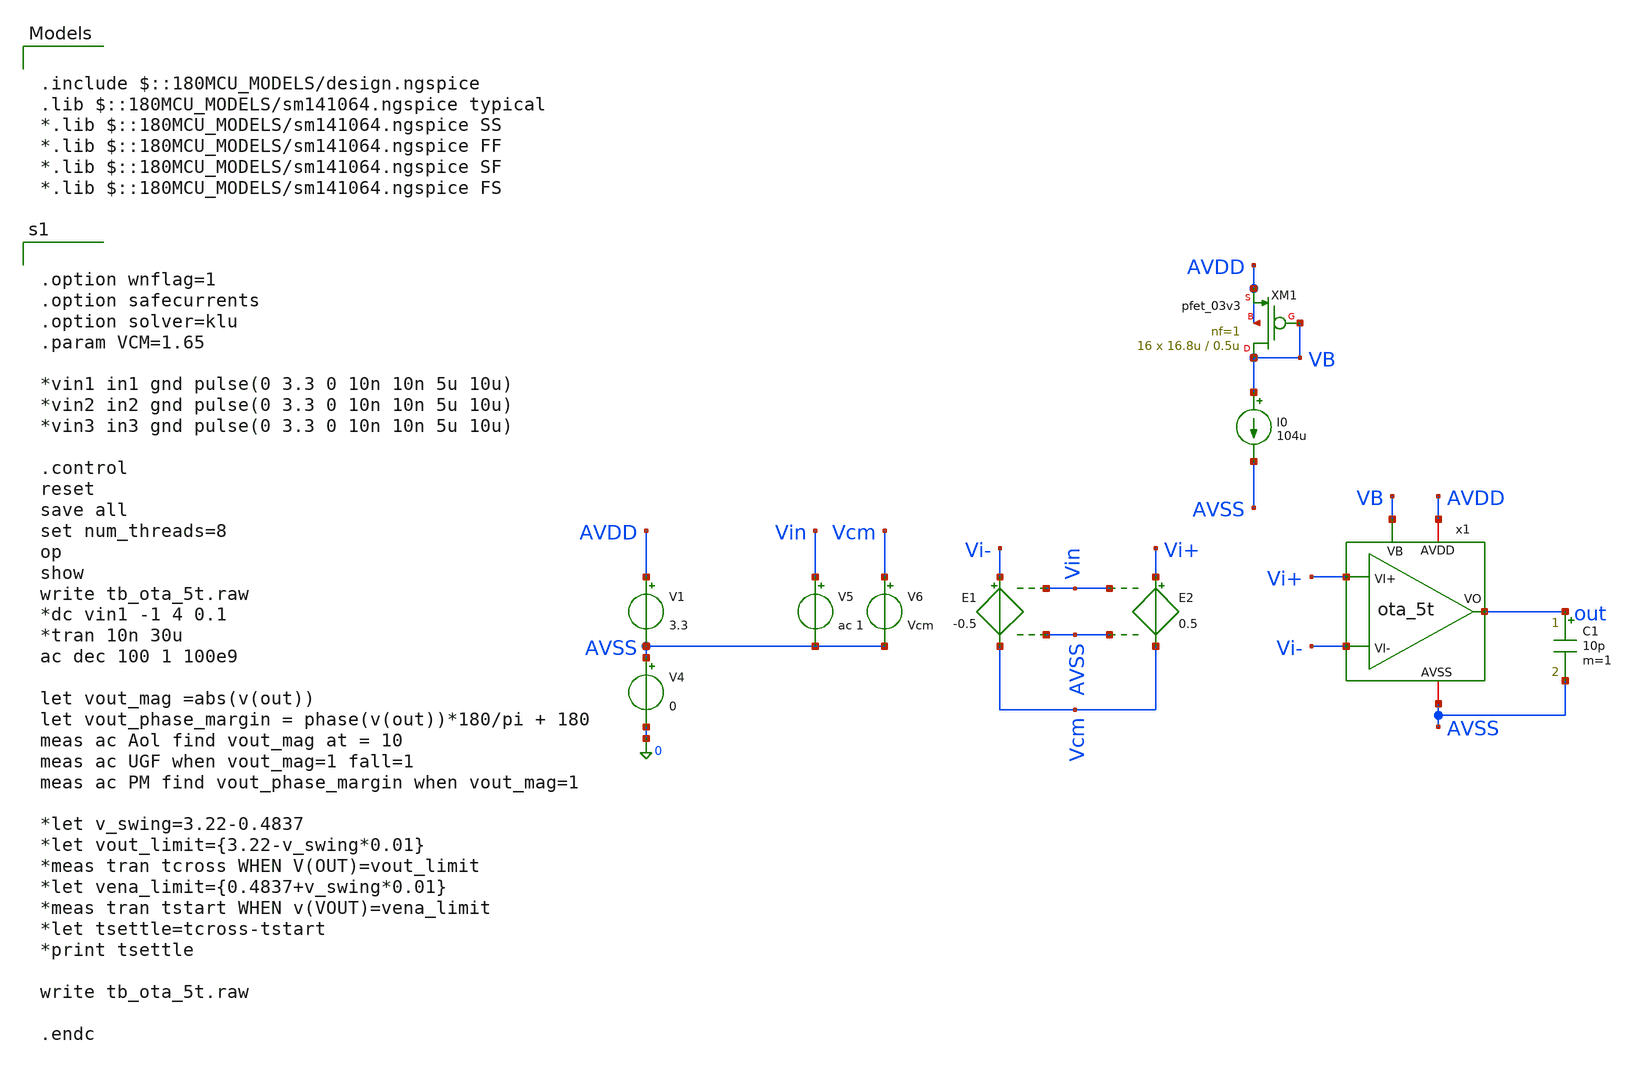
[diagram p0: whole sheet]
** sch_path: designs/libs/tb_analog/tb_ota_5t/tb_ota_5t.sch
**.subckt tb_ota_5t
x1 out AVDD Vi+ Vi- AVSS VB ota_5t
V1 AVDD AVSS 3.3
V4 AVSS 0 0
E1 Vi- Vcm Vin AVSS -0.5
E2 Vi+ Vcm Vin AVSS 0.5
V5 Vin AVSS ac 1
V6 Vcm AVSS Vcm
C1 out AVSS 10p m=1
I0 VB AVSS 104u
XM1 VB VB AVDD AVDD pfet_03v3 L=0.5u W=16.8u nf=1 ad='int((nf+1)/2) * W/nf * 0.18u' as='int((nf+2)/2) * W/nf * 0.18u'
+ pd='2*int((nf+1)/2) * (W/nf + 0.18u)' ps='2*int((nf+2)/2) * (W/nf + 0.18u)' nrd='0.18u / W' nrs='0.18u / W'
+ sa=0 sb=0 sd=0 m=16
**** begin user architecture code

.include $::180MCU_MODELS/design.ngspice
.lib $::180MCU_MODELS/sm141064.ngspice typical
*.lib $::180MCU_MODELS/sm141064.ngspice SS
*.lib $::180MCU_MODELS/sm141064.ngspice FF
*.lib $::180MCU_MODELS/sm141064.ngspice SF
*.lib $::180MCU_MODELS/sm141064.ngspice FS



.option wnflag=1
.option safecurrents
.option solver=klu
.param VCM=1.65

*vin1 in1 gnd pulse(0 3.3 0 10n 10n 5u 10u)
*vin2 in2 gnd pulse(0 3.3 0 10n 10n 5u 10u)
*vin3 in3 gnd pulse(0 3.3 0 10n 10n 5u 10u)

.control
reset
save all
set num_threads=8
op
show
write tb_ota_5t.raw
*dc vin1 -1 4 0.1
*tran 10n 30u
ac dec 100 1 100e9

let vout_mag =abs(v(out))
let vout_phase_margin = phase(v(out))*180/pi + 180
meas ac Aol find vout_mag at = 10
meas ac UGF when vout_mag=1 fall=1
meas ac PM find vout_phase_margin when vout_mag=1

*let v_swing=3.22-0.4837
*let vout_limit={3.22-v_swing*0.01}
*meas tran tcross WHEN V(OUT)=vout_limit
*let vena_limit={0.4837+v_swing*0.01}
*meas tran tstart WHEN v(VOUT)=vena_limit
*let tsettle=tcross-tstart
*print tsettle

write tb_ota_5t.raw

.endc


**** end user architecture code
**.ends

* expanding   symbol:  libs/core_analog/ota_5t/ota_5t.sym # of pins=6
** sym_path: designs/libs/core_analog/ota_5t/ota_5t.sym
** sch_path: designs/libs/core_analog/ota_5t/ota_5t.sch
.subckt ota_5t VO AVDD VI+ VI- AVSS VB
*.ipin VI+
*.ipin VI-
*.ipin VB
*.iopin AVDD
*.iopin AVSS
*.opin VO
XM1 VO VI- net2 AVDD pfet_03v3 L=0.5u W=6.55u nf=1 ad='int((nf+1)/2) * W/nf * 0.18u' as='int((nf+2)/2) * W/nf * 0.18u'
+ pd='2*int((nf+1)/2) * (W/nf + 0.18u)' ps='2*int((nf+2)/2) * (W/nf + 0.18u)' nrd='0.18u / W' nrs='0.18u / W'
+ sa=0 sb=0 sd=0 m=8
XM4 VO net1 AVSS AVSS nfet_03v3 L=0.5u W=4.8u nf=1 ad='int((nf+1)/2) * W/nf * 0.18u' as='int((nf+2)/2) * W/nf * 0.18u'
+ pd='2*int((nf+1)/2) * (W/nf + 0.18u)' ps='2*int((nf+2)/2) * (W/nf + 0.18u)' nrd='0.18u / W' nrs='0.18u / W'
+ sa=0 sb=0 sd=0 m=4
XM3 net2 VB net3 AVDD pfet_03v3 L=0.5u W=16.8u nf=1 ad='int((nf+1)/2) * W/nf * 0.18u' as='int((nf+2)/2) * W/nf * 0.18u'
+ pd='2*int((nf+1)/2) * (W/nf + 0.18u)' ps='2*int((nf+2)/2) * (W/nf + 0.18u)' nrd='0.18u / W' nrs='0.18u / W'
+ sa=0 sb=0 sd=0 m=16
XM2 net1 VI+ net2 AVDD pfet_03v3 L=0.5u W=6.55u nf=1 ad='int((nf+1)/2) * W/nf * 0.18u' as='int((nf+2)/2) * W/nf * 0.18u'
+ pd='2*int((nf+1)/2) * (W/nf + 0.18u)' ps='2*int((nf+2)/2) * (W/nf + 0.18u)' nrd='0.18u / W' nrs='0.18u / W'
+ sa=0 sb=0 sd=0 m=8
XM5 net1 net1 AVSS AVSS nfet_03v3 L=0.5u W=4.8u nf=1 ad='int((nf+1)/2) * W/nf * 0.18u' as='int((nf+2)/2) * W/nf * 0.18u'
+ pd='2*int((nf+1)/2) * (W/nf + 0.18u)' ps='2*int((nf+2)/2) * (W/nf + 0.18u)' nrd='0.18u / W' nrs='0.18u / W'
+ sa=0 sb=0 sd=0 m=4
Vmeas AVDD net3 0
.save i(vmeas)
.ends

.end
